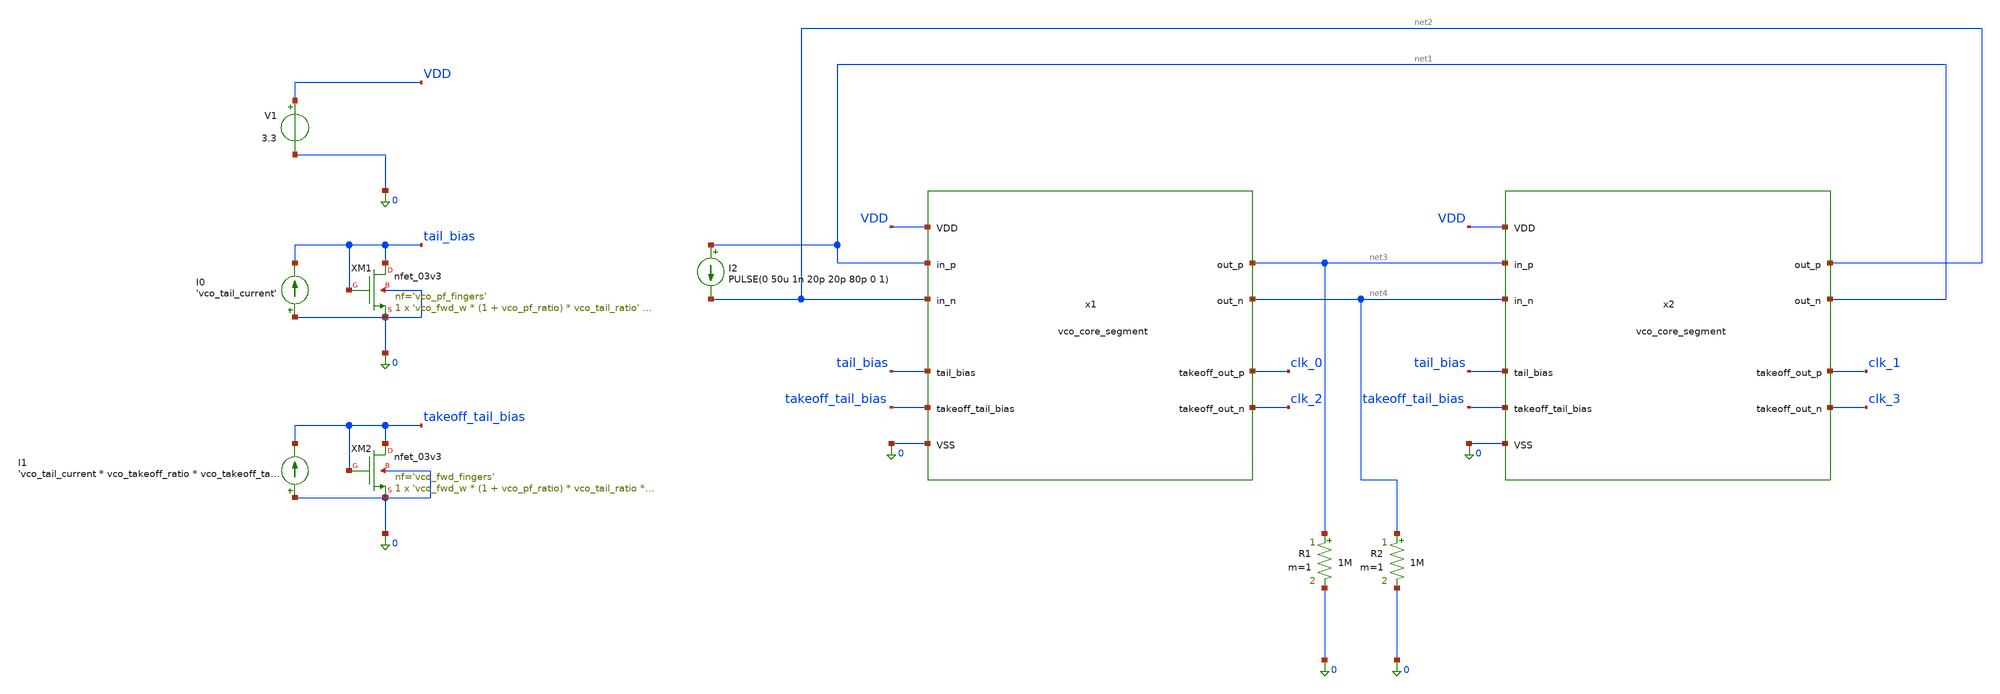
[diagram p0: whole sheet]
** sch_path: xschem/vco_core_tb.sch
**.subckt vco_core_tb
x1 0 VDD net4 net3 net1 net2 clk_2 clk_0 tail_bias takeoff_tail_bias vco_core_segment
XM1 tail_bias tail_bias 0 0 nfet_03v3 L='vco_tail_l' W='vco_fwd_w * (1 + vco_pf_ratio) * vco_tail_ratio'
+ nf='vco_pf_fingers' ad='int((nf+1)/2) * W/nf * 0.18u' as='int((nf+2)/2) * W/nf * 0.18u' pd='2*int((nf+1)/2) * (W/nf + 0.18u)'
+ ps='2*int((nf+2)/2) * (W/nf + 0.18u)' nrd='0.18u / W' nrs='0.18u / W' sa=0 sb=0 sd=0 m=1
x2 0 VDD net1 net2 net3 net4 clk_3 clk_1 tail_bias takeoff_tail_bias vco_core_segment
XM2 takeoff_tail_bias takeoff_tail_bias 0 0 nfet_03v3 L='vco_takeoff_tail_l' W='vco_fwd_w * (1 + vco_pf_ratio) * vco_tail_ratio * vco_takeoff_ratio'
+ nf='vco_fwd_fingers' ad='int((nf+1)/2) * W/nf * 0.18u' as='int((nf+2)/2) * W/nf * 0.18u' pd='2*int((nf+1)/2) * (W/nf + 0.18u)'
+ ps='2*int((nf+2)/2) * (W/nf + 0.18u)' nrd='0.18u / W' nrs='0.18u / W' sa=0 sb=0 sd=0 m=1
V1 VDD 0 3.3
I0 0 tail_bias 'vco_tail_current'
I1 0 takeoff_tail_bias 'vco_tail_current * vco_takeoff_ratio * vco_takeoff_tail_adjust'
I2 net1 net2 PULSE(0 50u 1n 20p 20p 80p 0 1)
R1 net3 0 1M m=1
R2 net4 0 1M m=1
**** begin user architecture code
 .include $::180MCU_MODELS/design.ngspice
.lib $::180MCU_MODELS/sm141064.ngspice typical
.lib $::180MCU_MODELS/sm141064.ngspice res_typical


.option savecurrents

.param vco_fwd_w=12u
.param vco_pf_S=1
.param vco_pf_ratio='1/vco_pf_S'
.param vco_fwd_fingers=3
.param vco_pf_fingers=3
.param vco_takeoff_ratio=1
.param vco_takeoff_fingers=6
.param vco_tail_ratio=5
.param vco_tail_l=0.5u
.param vco_takeoff_tail_ratio=5
.param vco_takeoff_tail_l=0.5u
.param vco_load_w=1u
.param vco_load_r=13k
.param vco_load_l='vco_load_r/1000 * vco_load_w'
.param vco_takeoff_load_adjust=1
.param vco_takeoff_load_w=1u
.param vco_takeoff_load_r='(vco_load_r / vco_takeoff_ratio) * vco_takeoff_load_adjust'
.param vco_takeoff_load_l='vco_takeoff_load_r/1000 * vco_takeoff_load_w'
.param vco_takeoff_tail_adjust=1
.param vco_tail_current=192u

.control
save all
tran 50p 5000n
plot v(clk_0) v(clk_1) v(clk_2) v(clk_3)
.endc
**** end user architecture code
**.ends
.end
